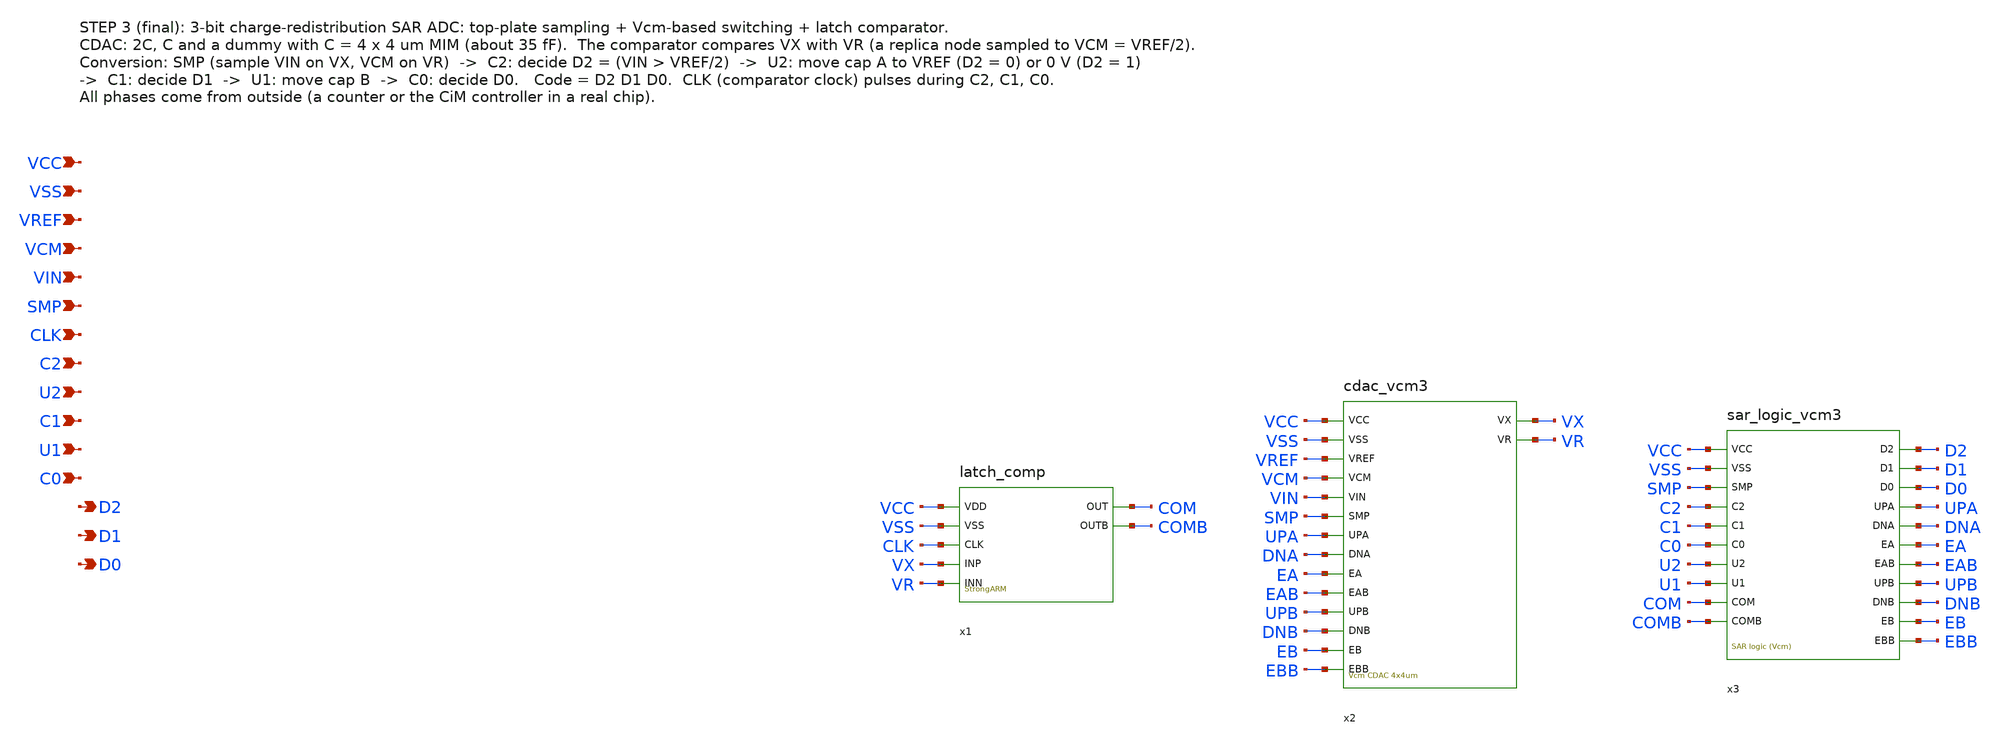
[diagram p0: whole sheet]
** sch_path: sar_adc3_v3.sch
**.subckt sar_adc3_v3 VCC VSS VREF VCM VIN SMP CLK C2 U2 C1 U1 C0 D2 D1 D0
*.ipin VCC
*.ipin VSS
*.ipin VREF
*.ipin VCM
*.ipin VIN
*.ipin SMP
*.ipin CLK
*.ipin C2
*.ipin U2
*.ipin C1
*.ipin U1
*.ipin C0
*.opin D2
*.opin D1
*.opin D0
x1 VCC VSS CLK VX VR COM COMB latch_comp
x2 VCC VSS VREF VCM VIN SMP UPA DNA EA EAB UPB DNB EB EBB VX VR cdac_vcm3
x3 VCC VSS SMP C2 C1 C0 U2 U1 COM COMB D2 D1 D0 UPA DNA EA EAB UPB DNB EB EBB sar_logic_vcm3
**.ends
.end
